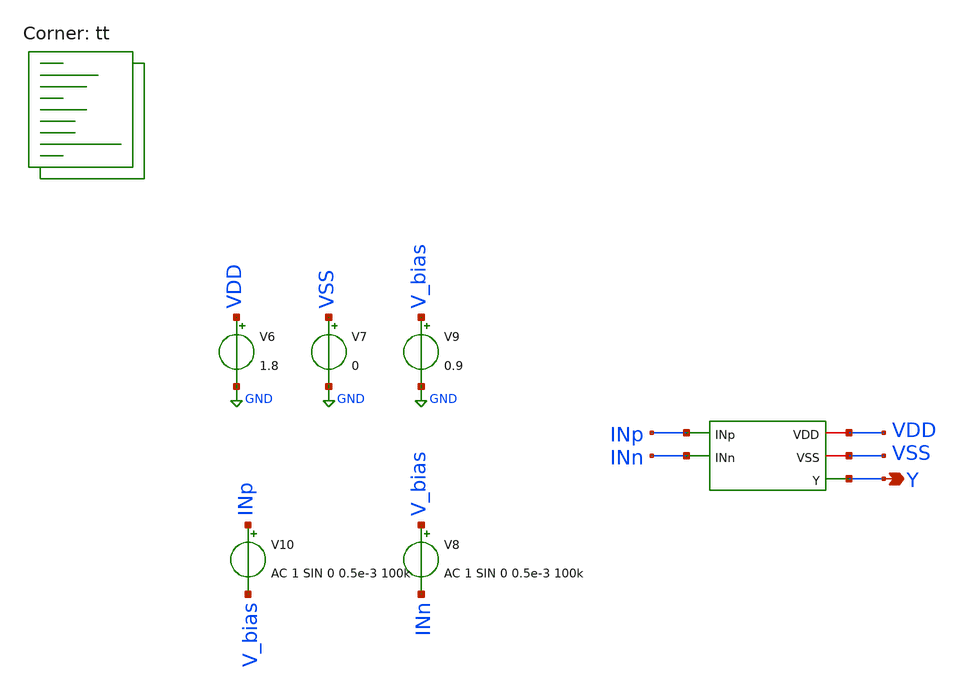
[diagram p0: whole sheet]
** sch_path: xschem/src/amp2_test.sch
**.subckt amp2_test Y
*.opin Y
V6 VDD GND 1.8
V7 VSS GND 0
V8 V_bias INn AC 1 SIN 0 0.5e-3 100k
V9 V_bias GND 0.9
V10 INp V_bias AC 1 SIN 0 0.5e-3 100k
x1 VDD VSS INp Y INn amp2
**** begin user architecture code
.lib $::SKYWATER_MODELS/sky130.lib.spice tt


* ngspice commands
.options list act
.options method=gear
.options savecurrents
.temp 25

.control
save all
*tran 1n 50u
ac dec 10 1 10e9

write amp2_test.raw
.endc



*.lib /foss/pdks/sky130/libs.tech/ngspice/sky130.lib.spice.tt
*.lib /foss/pdks/sky130/libs.tech/ngspice/sky130.lib.spice.ff
*.lib /foss/pdks/sky130/libs.tech/ngspice/sky130.lib.spice.ss

.include /foss/pdks/sky130A/libs.ref/sky130_fd_sc_hd/spice/sky130_fd_sc_hd.spice
*.include /foss/pdks/sky130A/libs.ref/sky130_fd_sc_pr/spice/sky130_fd_sc_pr.spice


**** end user architecture code
**.ends

* expanding   symbol:  xschem/src/amp2.sym # of pins=5
** sym_path: xschem/src/amp2.sym
** sch_path: xschem/src/amp2.sch
.subckt amp2 VDD VSS INp Y INn
*.opin Y
*.iopin VSS
*.ipin INp
*.ipin INn
*.iopin VDD
XM1 net1 net1 VDD VDD sky130_fd_pr__pfet_01v8 L=0.15 W=2 nf=4 ad='int((nf+1)/2) * W/nf * 0.29' as='int((nf+2)/2) * W/nf * 0.29'
+ pd='2*int((nf+1)/2) * (W/nf + 0.29)' ps='2*int((nf+2)/2) * (W/nf + 0.29)' nrd='0.29 / W' nrs='0.29 / W'
+ sa=0 sb=0 sd=0 mult=1 m=1
XM2 net1 INp net3 VSS sky130_fd_pr__nfet_01v8 L=0.15 W=2 nf=1 ad='int((nf+1)/2) * W/nf * 0.29' as='int((nf+2)/2) * W/nf * 0.29'
+ pd='2*int((nf+1)/2) * (W/nf + 0.29)' ps='2*int((nf+2)/2) * (W/nf + 0.29)' nrd='0.29 / W' nrs='0.29 / W'
+ sa=0 sb=0 sd=0 mult=1 m=1
XM3 net2 net1 VDD VDD sky130_fd_pr__pfet_01v8 L=0.15 W=2 nf=4 ad='int((nf+1)/2) * W/nf * 0.29' as='int((nf+2)/2) * W/nf * 0.29'
+ pd='2*int((nf+1)/2) * (W/nf + 0.29)' ps='2*int((nf+2)/2) * (W/nf + 0.29)' nrd='0.29 / W' nrs='0.29 / W'
+ sa=0 sb=0 sd=0 mult=1 m=1
XM4 Y net2 VDD VDD sky130_fd_pr__pfet_01v8 L=0.15 W=8 nf=2 ad='int((nf+1)/2) * W/nf * 0.29' as='int((nf+2)/2) * W/nf * 0.29'
+ pd='2*int((nf+1)/2) * (W/nf + 0.29)' ps='2*int((nf+2)/2) * (W/nf + 0.29)' nrd='0.29 / W' nrs='0.29 / W'
+ sa=0 sb=0 sd=0 mult=1 m=1
XM5 net2 INn net3 VSS sky130_fd_pr__nfet_01v8 L=0.15 W=2 nf=1 ad='int((nf+1)/2) * W/nf * 0.29' as='int((nf+2)/2) * W/nf * 0.29'
+ pd='2*int((nf+1)/2) * (W/nf + 0.29)' ps='2*int((nf+2)/2) * (W/nf + 0.29)' nrd='0.29 / W' nrs='0.29 / W'
+ sa=0 sb=0 sd=0 mult=1 m=1
XM6 net4 net4 VSS VSS sky130_fd_pr__nfet_01v8 L=0.15 W=2 nf=2 ad='int((nf+1)/2) * W/nf * 0.29' as='int((nf+2)/2) * W/nf * 0.29'
+ pd='2*int((nf+1)/2) * (W/nf + 0.29)' ps='2*int((nf+2)/2) * (W/nf + 0.29)' nrd='0.29 / W' nrs='0.29 / W'
+ sa=0 sb=0 sd=0 mult=1 m=1
XM7 net3 net4 VSS VSS sky130_fd_pr__nfet_01v8 L=0.15 W=2 nf=2 ad='int((nf+1)/2) * W/nf * 0.29' as='int((nf+2)/2) * W/nf * 0.29'
+ pd='2*int((nf+1)/2) * (W/nf + 0.29)' ps='2*int((nf+2)/2) * (W/nf + 0.29)' nrd='0.29 / W' nrs='0.29 / W'
+ sa=0 sb=0 sd=0 mult=1 m=1
XM8 Y net4 VSS VSS sky130_fd_pr__nfet_01v8 L=0.15 W=2 nf=2 ad='int((nf+1)/2) * W/nf * 0.29' as='int((nf+2)/2) * W/nf * 0.29'
+ pd='2*int((nf+1)/2) * (W/nf + 0.29)' ps='2*int((nf+2)/2) * (W/nf + 0.29)' nrd='0.29 / W' nrs='0.29 / W'
+ sa=0 sb=0 sd=0 mult=1 m=1
I0 VDD net4 200u
.ends

.GLOBAL GND
.end
